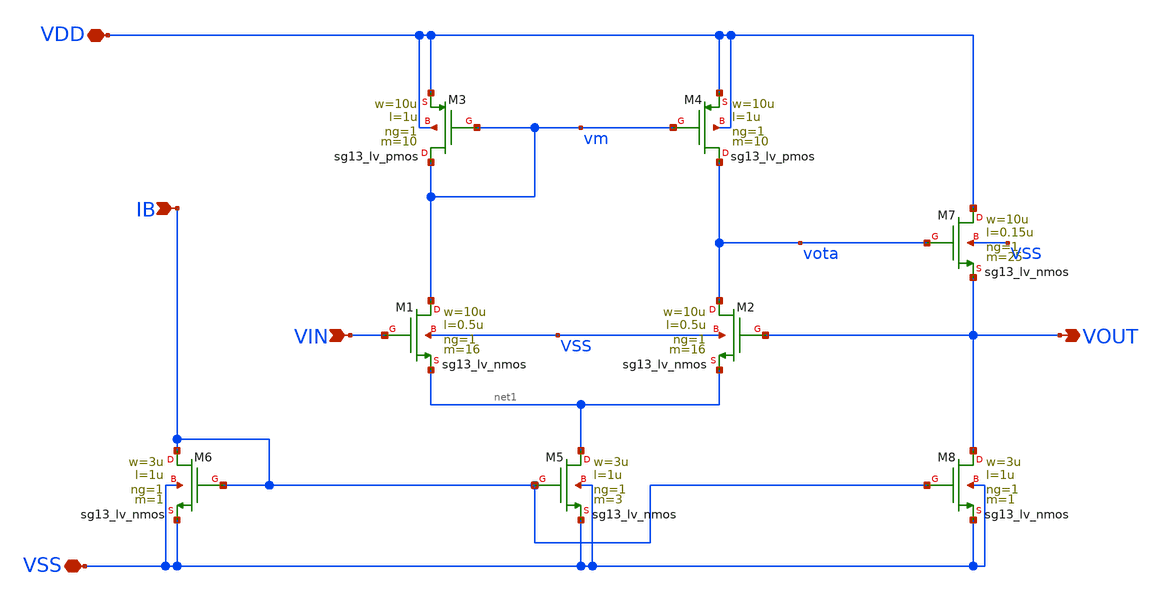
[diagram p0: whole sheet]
** sch_path: OTA_Telescopic/Schematics_and_Symbols/Buffer.sch
**.subckt Buffer VDD VSS VIN VOUT IB
*.iopin VDD
*.iopin VSS
*.ipin VIN
*.opin VOUT
*.ipin IB
XM5 net1 IB VSS VSS sg13_lv_nmos w=3u l=1u ng=1 m=3 mm_ok=1
XM6 IB IB VSS VSS sg13_lv_nmos w=3u l=1u ng=1 m=1 mm_ok=1
XM1 vm VIN net1 VSS sg13_lv_nmos w=10u l=0.5u ng=1 m=16 mm_ok=1
XM2 vota VOUT net1 VSS sg13_lv_nmos w=10u l=0.5u ng=1 m=16 mm_ok=1
XM3 vm vm VDD VDD sg13_lv_pmos w=10u l=1u ng=1 m=10 mm_ok=1
XM4 vota vm VDD VDD sg13_lv_pmos w=10u l=1u ng=1 m=10 mm_ok=1
XM7 VDD vota VOUT VSS sg13_lv_nmos w=10u l=0.15u ng=1 m=25 mm_ok=1
XM8 VOUT IB VSS VSS sg13_lv_nmos w=3u l=1u ng=1 m=1 mm_ok=1
**.ends
.end
